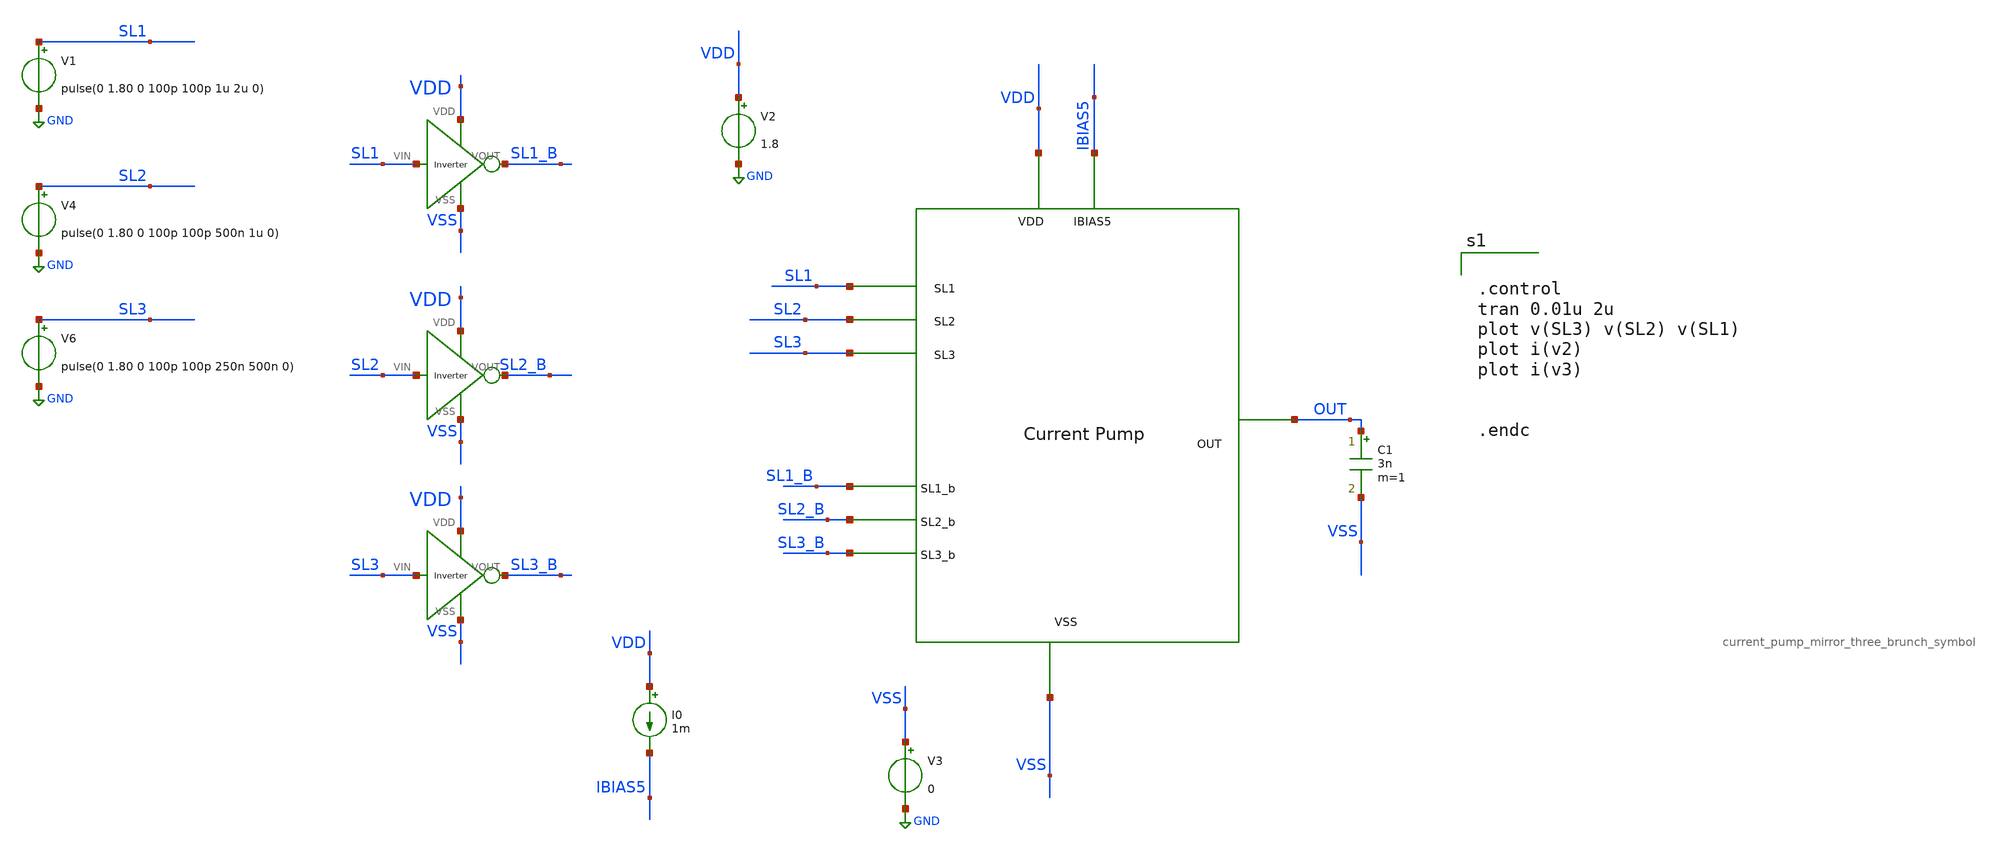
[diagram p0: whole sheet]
** sch_path: xschem/DC_DC_Converter_xschem/OTHERS/DC_DC_Converter_JV9/Current_pump_mirror/Current_pump_tb.sch
**.subckt Current_pump_tb
x1 VDD IBIAS5 SL3 OUT SL2 SL1 VSS SL3_B SL2_B SL1_B current_pump_mirror_three_brunch_symbol
V1 SL1 GND pulse(0 1.80 0 100p 100p 1u 2u 0)
V4 SL2 GND pulse(0 1.80 0 100p 100p 500n 1u 0)
V6 SL3 GND pulse(0 1.80 0 100p 100p 250n 500n 0)
V2 VDD GND 1.8
V3 VSS GND 0
I0 VDD IBIAS5 1m
C1 OUT VSS 3n m=1
X10 VSS VDD SL1 SL1_B Inverter
X1 VSS VDD SL2 SL2_B Inverter
X2 VSS VDD SL3 SL3_B Inverter
**** begin user architecture code


.control
tran 0.01u 2u
plot v(SL3) v(SL2) v(SL1)
plot i(v2)
plot i(v3)


.endc



** opencircuitdesign pdks install
.lib $::SKYWATER_MODELS/sky130.lib.spice tt
.include $::SKYWATER_STDCELLS/sky130_fd_sc_hd.spice


**** end user architecture code
**.ends
.GLOBAL GND
.end
